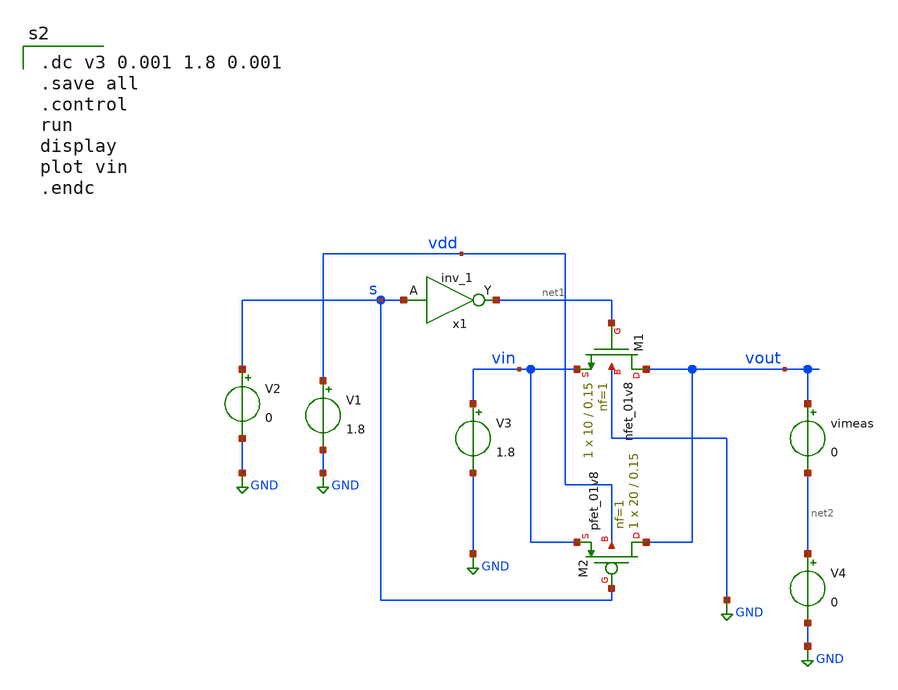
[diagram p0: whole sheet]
** sch_path: xschem/tgate_test.sch
**.subckt tgate_test
XM1 vout net1 vin GND sky130_fd_pr__nfet_01v8 L=0.15 W=10 nf=1 ad='int((nf+1)/2) * W/nf * 0.29' as='int((nf+2)/2) * W/nf * 0.29'
+ pd='2*int((nf+1)/2) * (W/nf + 0.29)' ps='2*int((nf+2)/2) * (W/nf + 0.29)' nrd='0.29 / W' nrs='0.29 / W'
+ sa=0 sb=0 sd=0 mult=1 m=1
XM2 vout s vin vdd sky130_fd_pr__pfet_01v8 L=0.15 W=20 nf=1 ad='int((nf+1)/2) * W/nf * 0.29' as='int((nf+2)/2) * W/nf * 0.29'
+ pd='2*int((nf+1)/2) * (W/nf + 0.29)' ps='2*int((nf+2)/2) * (W/nf + 0.29)' nrd='0.29 / W' nrs='0.29 / W'
+ sa=0 sb=0 sd=0 mult=1 m=1
V1 vdd GND 1.8
x1 s gnd gnd vdd vdd net1 sky130_fd_sc_hd__inv_1
V2 s GND 0
V3 vin GND 1.8
vimeas vout net2 0
V4 net2 GND 0
**** begin user architecture code
.lib $::SKYWATER_MODELS/sky130.lib.spice tt
.include $::PDKPATH/libs.ref/sky130_fd_sc_hd/spice/sky130_fd_sc_hd.spice


.dc v3 0.001 1.8 0.001
.save all
.control
run
display
plot vin
.endc


**** end user architecture code
**.ends
.GLOBAL GND
.end
